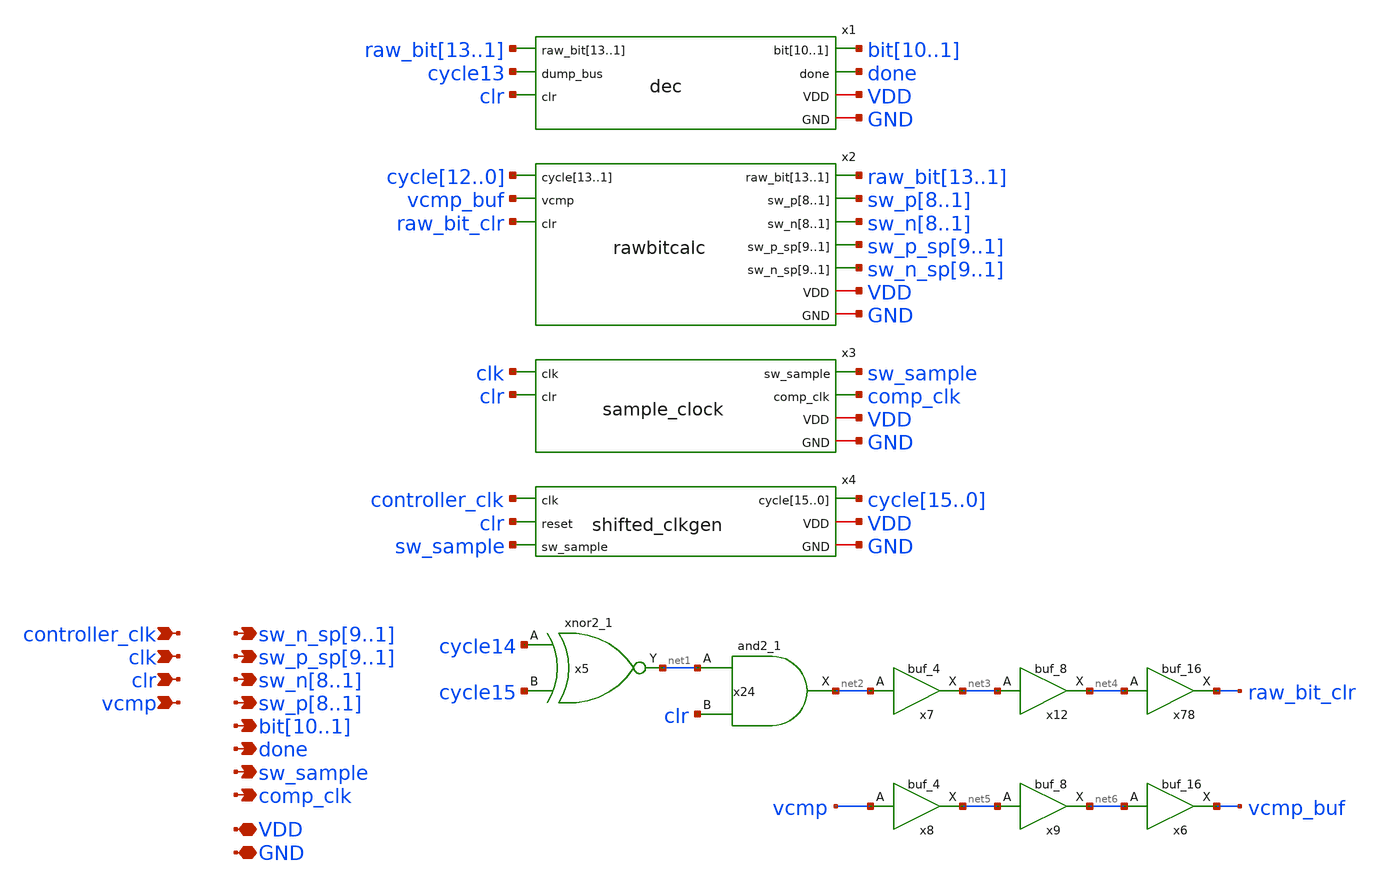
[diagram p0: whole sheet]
** sch_path: xschem/controller/controller.sch
**.subckt controller clk vcmp VDD GND clr controller_clk
*+ sw_n_sp9,sw_n_sp8,sw_n_sp7,sw_n_sp6,sw_n_sp5,sw_n_sp4,sw_n_sp3,sw_n_sp2,sw_n_sp1 sw_p_sp9,sw_p_sp8,sw_p_sp7,sw_p_sp6,sw_p_sp5,sw_p_sp4,sw_p_sp3,sw_p_sp2,sw_p_sp1
*+ sw_p8,sw_p7,sw_p6,sw_p5,sw_p4,sw_p3,sw_p2,sw_p1 sw_n8,sw_n7,sw_n6,sw_n5,sw_n4,sw_n3,sw_n2,sw_n1 bit10,bit9,bit8,bit7,bit6,bit5,bit4,bit3,bit2,bit1
*+ done sw_sample comp_clk
*.ipin clk
*.ipin vcmp
*.iopin VDD
*.iopin GND
*.ipin clr
*.ipin controller_clk
*.opin sw_n_sp9,sw_n_sp8,sw_n_sp7,sw_n_sp6,sw_n_sp5,sw_n_sp4,sw_n_sp3,sw_n_sp2,sw_n_sp1
*.opin sw_p_sp9,sw_p_sp8,sw_p_sp7,sw_p_sp6,sw_p_sp5,sw_p_sp4,sw_p_sp3,sw_p_sp2,sw_p_sp1
*.opin sw_p8,sw_p7,sw_p6,sw_p5,sw_p4,sw_p3,sw_p2,sw_p1
*.opin sw_n8,sw_n7,sw_n6,sw_n5,sw_n4,sw_n3,sw_n2,sw_n1
*.opin bit10,bit9,bit8,bit7,bit6,bit5,bit4,bit3,bit2,bit1
*.opin done
*.opin sw_sample
*.opin comp_clk
x1 bit10 bit9 bit8 bit7 bit6 bit5 bit4 bit3 bit2 bit1 raw_bit13 raw_bit12 raw_bit11 raw_bit10
+ raw_bit9 raw_bit8 raw_bit7 raw_bit6 raw_bit5 raw_bit4 raw_bit3 raw_bit2 raw_bit1 cycle13 done clr VDD GND
+ dec
x2 raw_bit13 raw_bit12 raw_bit11 raw_bit10 raw_bit9 raw_bit8 raw_bit7 raw_bit6 raw_bit5 raw_bit4
+ raw_bit3 raw_bit2 raw_bit1 cycle12 cycle11 cycle10 cycle9 cycle8 cycle7 cycle6 cycle5 cycle4 cycle3 cycle2
+ cycle1 cycle0 vcmp_buf sw_p8 sw_p7 sw_p6 sw_p5 sw_p4 sw_p3 sw_p2 sw_p1 sw_n8 sw_n7 sw_n6 sw_n5 sw_n4 sw_n3
+ sw_n2 sw_n1 raw_bit_clr sw_p_sp9 sw_p_sp8 sw_p_sp7 sw_p_sp6 sw_p_sp5 sw_p_sp4 sw_p_sp3 sw_p_sp2 sw_p_sp1
+ sw_n_sp9 sw_n_sp8 sw_n_sp7 sw_n_sp6 sw_n_sp5 sw_n_sp4 sw_n_sp3 sw_n_sp2 sw_n_sp1 VDD GND rawbitcalc
x3 sw_sample clk clr comp_clk VDD GND sample_clock
x4 controller_clk cycle15 cycle14 cycle13 cycle12 cycle11 cycle10 cycle9 cycle8 cycle7 cycle6 cycle5
+ cycle4 cycle3 cycle2 cycle1 cycle0 clr sw_sample VDD GND shifted_clkgen
x5 cycle14 cycle15 GND GND VDD VDD net1 sky130_fd_sc_hd__xnor2_1
x24 net1 clr GND GND VDD VDD net2 sky130_fd_sc_hd__and2_1
x78 net4 GND GND VDD VDD raw_bit_clr sky130_fd_sc_hd__buf_16
x7 net2 GND GND VDD VDD net3 sky130_fd_sc_hd__buf_4
x12 net3 GND GND VDD VDD net4 sky130_fd_sc_hd__buf_8
x6 net6 GND GND VDD VDD vcmp_buf sky130_fd_sc_hd__buf_16
x8 vcmp GND GND VDD VDD net5 sky130_fd_sc_hd__buf_4
x9 net5 GND GND VDD VDD net6 sky130_fd_sc_hd__buf_8
**.ends
.end
